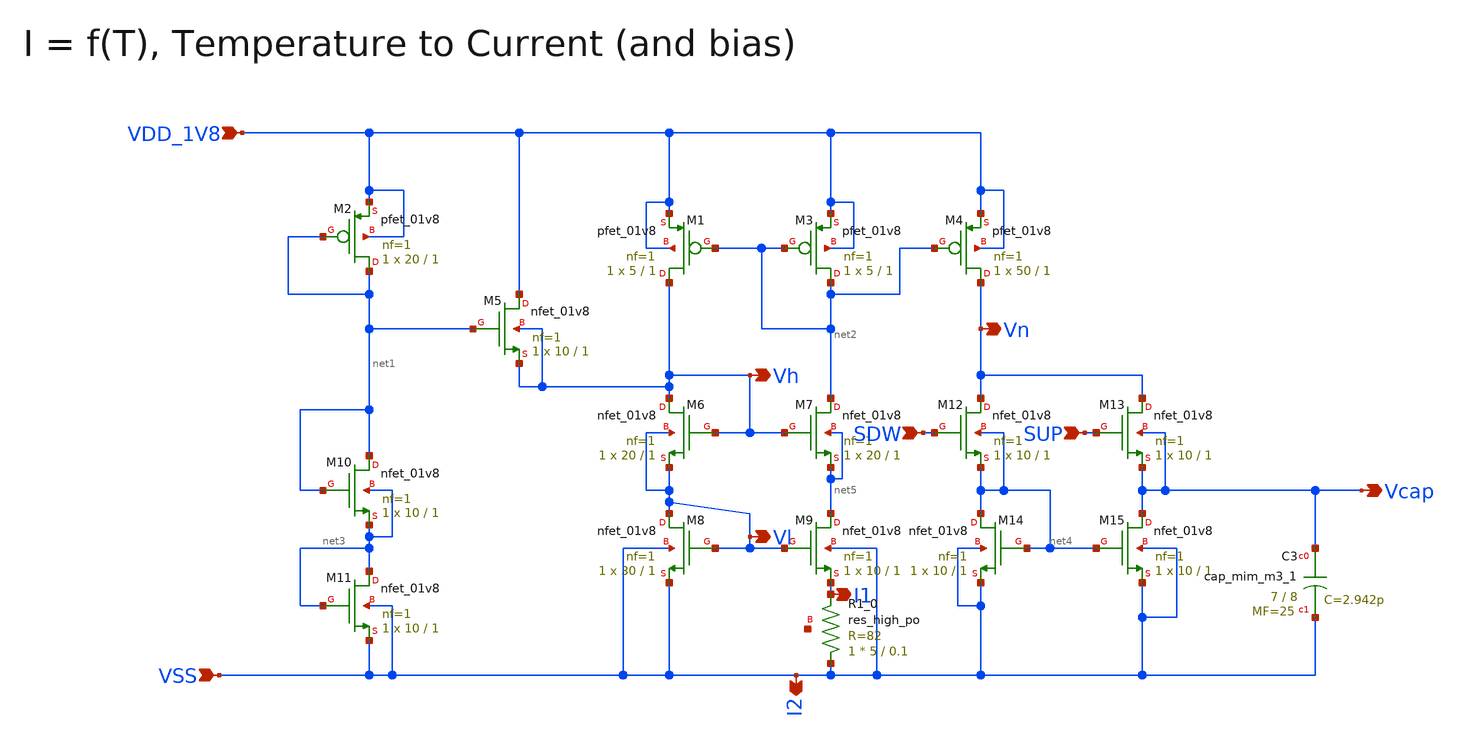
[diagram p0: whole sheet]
** sch_path: design/CNR_GR06_SKY130NM/CNR_GR06.sch
**.subckt CNR_GR06 VDD_1V8 VSS I2 I1 Vn Vcap SUP SDW Vh Vl
*.ipin VDD_1V8
*.ipin VSS
*.opin I2
*.opin I1
*.opin Vn
*.opin Vcap
*.ipin SUP
*.ipin SDW
*.opin Vh
*.opin Vl
XM5 VDD_1V8 net1 Vh Vh sky130_fd_pr__nfet_01v8 L=1 W=10 nf=1 ad='int((nf+1)/2) * W/nf * 0.29' as='int((nf+2)/2) * W/nf * 0.29'
+ pd='2*int((nf+1)/2) * (W/nf + 0.29)' ps='2*int((nf+2)/2) * (W/nf + 0.29)' nrd='0.29 / W' nrs='0.29 / W'
+ sa=0 sb=0 sd=0 mult=1 m=1
XM2 net1 net1 VDD_1V8 VDD_1V8 sky130_fd_pr__pfet_01v8 L=1 W=20 nf=1 ad='int((nf+1)/2) * W/nf * 0.29'
+ as='int((nf+2)/2) * W/nf * 0.29' pd='2*int((nf+1)/2) * (W/nf + 0.29)' ps='2*int((nf+2)/2) * (W/nf + 0.29)'
+ nrd='0.29 / W' nrs='0.29 / W' sa=0 sb=0 sd=0 mult=1 m=1
XM1 Vh net2 VDD_1V8 VDD_1V8 sky130_fd_pr__pfet_01v8 L=1 W=5 nf=1 ad='int((nf+1)/2) * W/nf * 0.29' as='int((nf+2)/2) * W/nf * 0.29'
+ pd='2*int((nf+1)/2) * (W/nf + 0.29)' ps='2*int((nf+2)/2) * (W/nf + 0.29)' nrd='0.29 / W' nrs='0.29 / W'
+ sa=0 sb=0 sd=0 mult=1 m=1
XM3 net2 net2 VDD_1V8 VDD_1V8 sky130_fd_pr__pfet_01v8 L=1 W=5 nf=1 ad='int((nf+1)/2) * W/nf * 0.29' as='int((nf+2)/2) * W/nf * 0.29'
+ pd='2*int((nf+1)/2) * (W/nf + 0.29)' ps='2*int((nf+2)/2) * (W/nf + 0.29)' nrd='0.29 / W' nrs='0.29 / W'
+ sa=0 sb=0 sd=0 mult=1 m=1
XM4 Vn net2 VDD_1V8 VDD_1V8 sky130_fd_pr__pfet_01v8 L=1 W=50 nf=1 ad='int((nf+1)/2) * W/nf * 0.29' as='int((nf+2)/2) * W/nf * 0.29'
+ pd='2*int((nf+1)/2) * (W/nf + 0.29)' ps='2*int((nf+2)/2) * (W/nf + 0.29)' nrd='0.29 / W' nrs='0.29 / W'
+ sa=0 sb=0 sd=0 mult=1 m=1
XM6 Vh Vh Vl Vl sky130_fd_pr__nfet_01v8 L=1 W=20 nf=1 ad='int((nf+1)/2) * W/nf * 0.29' as='int((nf+2)/2) * W/nf * 0.29'
+ pd='2*int((nf+1)/2) * (W/nf + 0.29)' ps='2*int((nf+2)/2) * (W/nf + 0.29)' nrd='0.29 / W' nrs='0.29 / W'
+ sa=0 sb=0 sd=0 mult=1 m=1
XM7 net2 Vh net5 net5 sky130_fd_pr__nfet_01v8 L=1 W=20 nf=1 ad='int((nf+1)/2) * W/nf * 0.29' as='int((nf+2)/2) * W/nf * 0.29'
+ pd='2*int((nf+1)/2) * (W/nf + 0.29)' ps='2*int((nf+2)/2) * (W/nf + 0.29)' nrd='0.29 / W' nrs='0.29 / W'
+ sa=0 sb=0 sd=0 mult=1 m=1
XM8 Vl Vl VSS VSS sky130_fd_pr__nfet_01v8 L=1 W=30 nf=1 ad='int((nf+1)/2) * W/nf * 0.29' as='int((nf+2)/2) * W/nf * 0.29'
+ pd='2*int((nf+1)/2) * (W/nf + 0.29)' ps='2*int((nf+2)/2) * (W/nf + 0.29)' nrd='0.29 / W' nrs='0.29 / W'
+ sa=0 sb=0 sd=0 mult=1 m=1
XM9 net5 Vl I1 VSS sky130_fd_pr__nfet_01v8 L=1 W=10 nf=1 ad='int((nf+1)/2) * W/nf * 0.29' as='int((nf+2)/2) * W/nf * 0.29'
+ pd='2*int((nf+1)/2) * (W/nf + 0.29)' ps='2*int((nf+2)/2) * (W/nf + 0.29)' nrd='0.29 / W' nrs='0.29 / W'
+ sa=0 sb=0 sd=0 mult=1 m=1
XM10 net1 net1 net3 net3 sky130_fd_pr__nfet_01v8 L=1 W=10 nf=1 ad='int((nf+1)/2) * W/nf * 0.29' as='int((nf+2)/2) * W/nf * 0.29'
+ pd='2*int((nf+1)/2) * (W/nf + 0.29)' ps='2*int((nf+2)/2) * (W/nf + 0.29)' nrd='0.29 / W' nrs='0.29 / W'
+ sa=0 sb=0 sd=0 mult=1 m=1
XM11 net3 net3 VSS VSS sky130_fd_pr__nfet_01v8 L=1 W=10 nf=1 ad='int((nf+1)/2) * W/nf * 0.29' as='int((nf+2)/2) * W/nf * 0.29'
+ pd='2*int((nf+1)/2) * (W/nf + 0.29)' ps='2*int((nf+2)/2) * (W/nf + 0.29)' nrd='0.29 / W' nrs='0.29 / W'
+ sa=0 sb=0 sd=0 mult=1 m=1
XM12 Vn SDW net4 net4 sky130_fd_pr__nfet_01v8 L=1 W=10 nf=1 ad='int((nf+1)/2) * W/nf * 0.29' as='int((nf+2)/2) * W/nf * 0.29'
+ pd='2*int((nf+1)/2) * (W/nf + 0.29)' ps='2*int((nf+2)/2) * (W/nf + 0.29)' nrd='0.29 / W' nrs='0.29 / W'
+ sa=0 sb=0 sd=0 mult=1 m=1
XM13 Vn SUP Vcap Vcap sky130_fd_pr__nfet_01v8 L=1 W=10 nf=1 ad='int((nf+1)/2) * W/nf * 0.29' as='int((nf+2)/2) * W/nf * 0.29'
+ pd='2*int((nf+1)/2) * (W/nf + 0.29)' ps='2*int((nf+2)/2) * (W/nf + 0.29)' nrd='0.29 / W' nrs='0.29 / W'
+ sa=0 sb=0 sd=0 mult=1 m=1
XM14 net4 net4 VSS VSS sky130_fd_pr__nfet_01v8 L=1 W=10 nf=1 ad='int((nf+1)/2) * W/nf * 0.29' as='int((nf+2)/2) * W/nf * 0.29'
+ pd='2*int((nf+1)/2) * (W/nf + 0.29)' ps='2*int((nf+2)/2) * (W/nf + 0.29)' nrd='0.29 / W' nrs='0.29 / W'
+ sa=0 sb=0 sd=0 mult=1 m=1
XM15 Vcap net4 VSS VSS sky130_fd_pr__nfet_01v8 L=1 W=10 nf=1 ad='int((nf+1)/2) * W/nf * 0.29' as='int((nf+2)/2) * W/nf * 0.29'
+ pd='2*int((nf+1)/2) * (W/nf + 0.29)' ps='2*int((nf+2)/2) * (W/nf + 0.29)' nrd='0.29 / W' nrs='0.29 / W'
+ sa=0 sb=0 sd=0 mult=1 m=1
XC3 Vcap VSS sky130_fd_pr__cap_mim_m3_1 W=7 L=8 MF=25 m=25
XR1_0 VSS I1 net6 sky130_fd_pr__res_high_po W=5 L=0.1 mult=1 m=1
**.ends
.end
